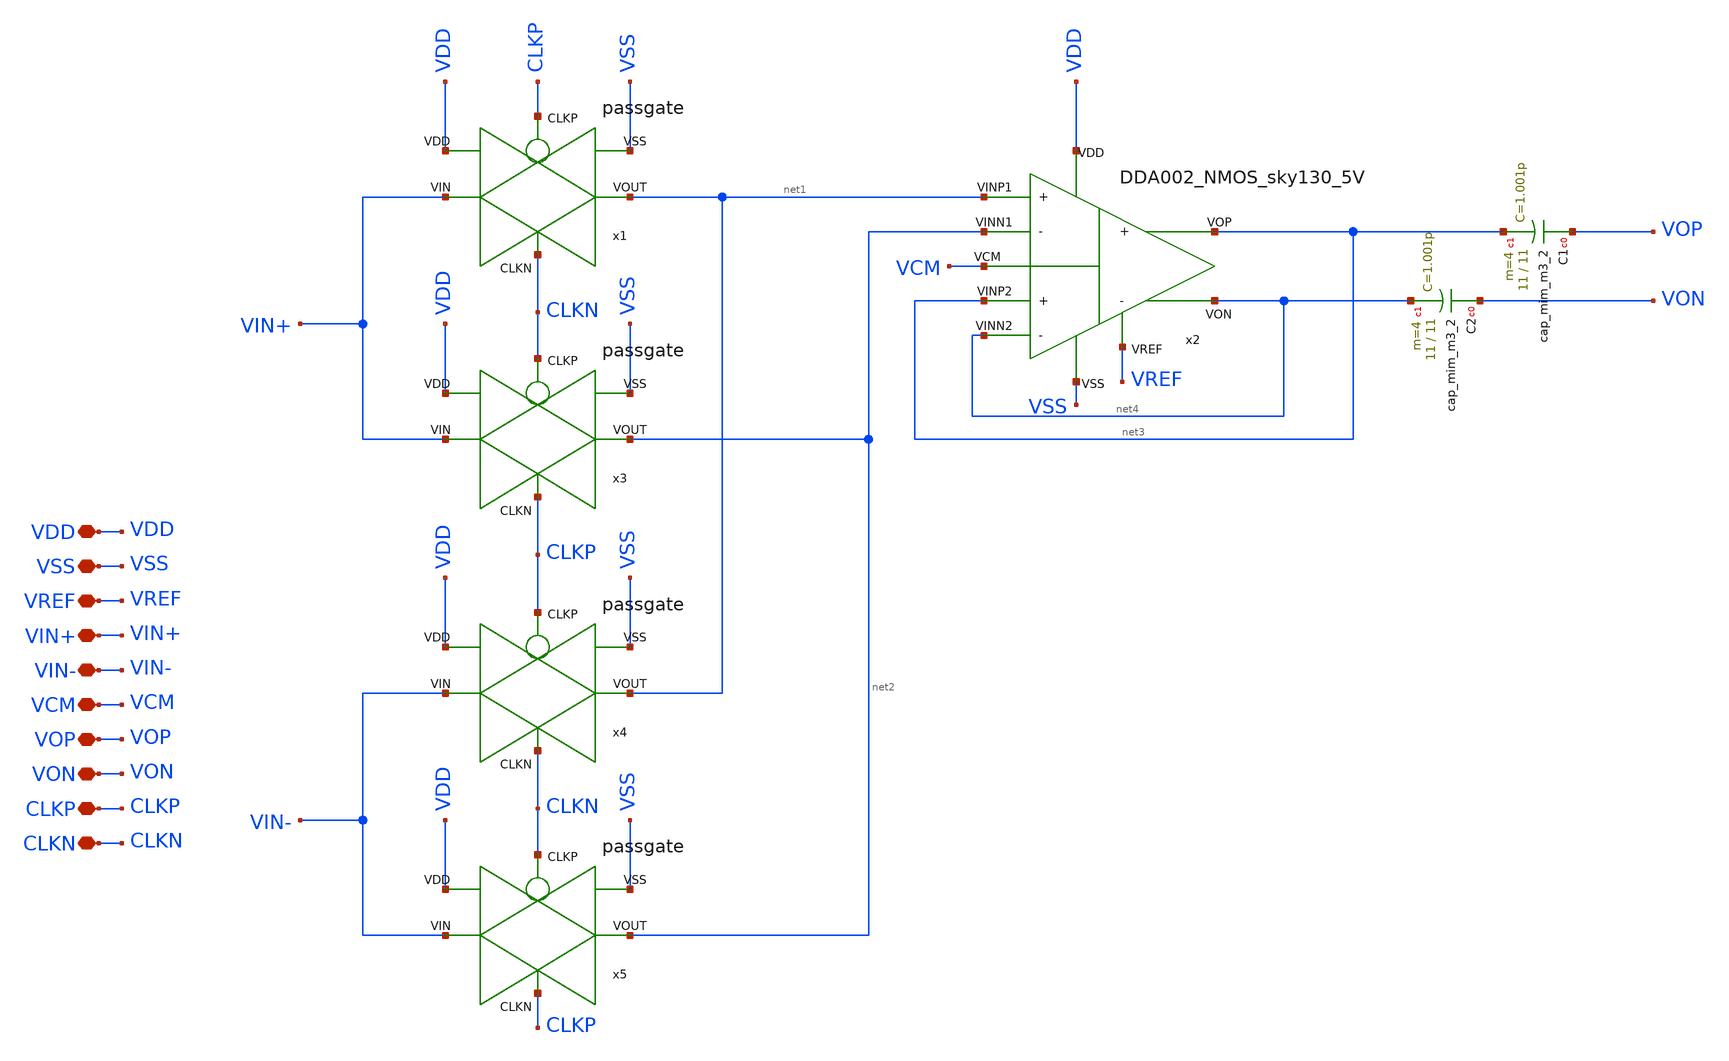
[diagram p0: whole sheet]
** sch_path: LIB/Sky130A/chopping/5v_sampling_chopping_buffer.sch
**.subckt 5v_sampling_chopping_buffer VDD VSS VREF VIN+ VIN- VCM VOP VON CLKP CLKN
*.iopin VDD
*.iopin VSS
*.iopin VREF
*.iopin VIN+
*.iopin VIN-
*.iopin VCM
*.iopin VOP
*.iopin VON
*.iopin CLKP
*.iopin CLKN
x2 VDD VSS VREF net2 net4 net1 net3 VCM net3 net4 DDA002_NMOS_sky130_5V
x1 VDD VSS VIN+ net1 CLKP CLKN passgate
x3 VDD VSS VIN+ net2 CLKN CLKP passgate
x4 VDD VSS VIN- net1 CLKP CLKN passgate
x5 VDD VSS VIN- net2 CLKN CLKP passgate
XC2 VON net4 sky130_fd_pr__cap_mim_m3_2 W=11 L=11 MF=4 m=4
XC1 VOP net3 sky130_fd_pr__cap_mim_m3_2 W=11 L=11 MF=4 m=4
**.ends

* expanding   symbol:  Sky130A/DDA/DDA002_NMOS_sky130_5V.sym # of pins=10
** sym_path: LIB/Sky130A/DDA/DDA002_NMOS_sky130_5V.sym
** sch_path: LIB/Sky130A/DDA/DDA002_NMOS_sky130_5V.sch
.subckt DDA002_NMOS_sky130_5V VDD VSS VREF VINN1 VINN2 VINP1 VINP2 VCM VOP VON
*.iopin VDD
*.iopin VSS
*.iopin VREF
*.iopin VINN1
*.iopin VINN2
*.iopin VINP1
*.iopin VINP2
*.iopin VCM
*.iopin VOP
*.iopin VON
XM2 VA2 VCMFB VDD VDD sky130_fd_pr__pfet_g5v0d10v5 L=2 W='1 * 2 ' nf=2 ad='int((2 + 1)/2) * 1 * 0.29'
+ as='int((2 + 2)/2) * 1 * 0.29' pd='2*int((2 + 1)/2) * (1 + 0.29)' ps='2*int((2 + 2)/2) * (1 + 0.29)'
+ nrd='0.29 / 1 / 2 ' nrs='0.29 / 1 / 2 ' sa=0 sb=0 sd=0 mult=2 m=2
XM3 VA1 VINP1 net1 VSS sky130_fd_pr__nfet_g5v0d10v5 L=1 W='3 * 2 ' nf=2 ad='int((nf+1)/2) * W / nf * 0.29'
+ as='int((nf+2)/2) * W / nf * 0.29' pd='2*int((nf+1)/2) * (W / nf + 0.29)' ps='2*int((nf+2)/2) * (W / nf + 0.29)'
+ nrd='0.29 / W ' nrs='0.29 / W ' sa=0 sb=0 sd=0 mult=4 m=4
XM13 net3 VB VSS VSS sky130_fd_pr__nfet_g5v0d10v5 L=3 W='1 * 2 ' nf=2 ad='int((nf+1)/2) * W / nf * 0.29'
+ as='int((nf+2)/2) * W / nf * 0.29' pd='2*int((nf+1)/2) * (W / nf + 0.29)' ps='2*int((nf+2)/2) * (W / nf + 0.29)'
+ nrd='0.29 / W ' nrs='0.29 / W ' sa=0 sb=0 sd=0 mult=2 m=2
XR1 net3 VB VSS sky130_fd_pr__res_high_po_0p35 L=26 mult=1 m=1
XM14 VB VREF VDD VDD sky130_fd_pr__pfet_g5v0d10v5 L=2.5 W='1 * 2 ' nf=2 ad='int((2 + 1)/2) * 1 * 0.29'
+ as='int((2 + 2)/2) * 1 * 0.29' pd='2*int((2 + 1)/2) * (1 + 0.29)' ps='2*int((2 + 2)/2) * (1 + 0.29)'
+ nrd='0.29 / 1 / 2 ' nrs='0.29 / 1 / 2 ' sa=0 sb=0 sd=0 mult=2 m=2
XM7 net1 VB VSS VSS sky130_fd_pr__nfet_g5v0d10v5 L=3 W='1 * 2 ' nf=2 ad='int((nf+1)/2) * W / nf * 0.29'
+ as='int((nf+2)/2) * W / nf * 0.29' pd='2*int((nf+1)/2) * (W / nf + 0.29)' ps='2*int((nf+2)/2) * (W / nf + 0.29)'
+ nrd='0.29 / W ' nrs='0.29 / W ' sa=0 sb=0 sd=0 mult=2 m=2
XM8 net2 VB VSS VSS sky130_fd_pr__nfet_g5v0d10v5 L=3 W='1 * 2 ' nf=2 ad='int((nf+1)/2) * W / nf * 0.29'
+ as='int((nf+2)/2) * W / nf * 0.29' pd='2*int((nf+1)/2) * (W / nf + 0.29)' ps='2*int((nf+2)/2) * (W / nf + 0.29)'
+ nrd='0.29 / W ' nrs='0.29 / W ' sa=0 sb=0 sd=0 mult=2 m=2
XM10 VON VB VSS VSS sky130_fd_pr__nfet_g5v0d10v5 L=3 W='1 * 2 ' nf=2 ad='int((nf+1)/2) * W / nf * 0.29'
+ as='int((nf+2)/2) * W / nf * 0.29' pd='2*int((nf+1)/2) * (W / nf + 0.29)' ps='2*int((nf+2)/2) * (W / nf + 0.29)'
+ nrd='0.29 / W ' nrs='0.29 / W ' sa=0 sb=0 sd=0 mult=4 m=4
XM12 VOP VB VSS VSS sky130_fd_pr__nfet_g5v0d10v5 L=3 W='1 * 2 ' nf=2 ad='int((nf+1)/2) * W / nf * 0.29'
+ as='int((nf+2)/2) * W / nf * 0.29' pd='2*int((nf+1)/2) * (W / nf + 0.29)' ps='2*int((nf+2)/2) * (W / nf + 0.29)'
+ nrd='0.29 / W ' nrs='0.29 / W ' sa=0 sb=0 sd=0 mult=4 m=4
XM1 VA1 VCMFB VDD VDD sky130_fd_pr__pfet_g5v0d10v5 L=2 W='1 * 2 ' nf=2 ad='int((2 + 1)/2) * 1 * 0.29'
+ as='int((2 + 2)/2) * 1 * 0.29' pd='2*int((2 + 1)/2) * (1 + 0.29)' ps='2*int((2 + 2)/2) * (1 + 0.29)'
+ nrd='0.29 / 1 / 2 ' nrs='0.29 / 1 / 2 ' sa=0 sb=0 sd=0 mult=2 m=2
XM6 VA2 VINN1 net1 VSS sky130_fd_pr__nfet_g5v0d10v5 L=1 W='3 * 2 ' nf=2 ad='int((nf+1)/2) * W / nf * 0.29'
+ as='int((nf+2)/2) * W / nf * 0.29' pd='2*int((nf+1)/2) * (W / nf + 0.29)' ps='2*int((nf+2)/2) * (W / nf + 0.29)'
+ nrd='0.29 / W ' nrs='0.29 / W ' sa=0 sb=0 sd=0 mult=4 m=4
XM5 VA2 VINN2 net2 VSS sky130_fd_pr__nfet_g5v0d10v5 L=1 W='3 * 2 ' nf=2 ad='int((nf+1)/2) * W / nf * 0.29'
+ as='int((nf+2)/2) * W / nf * 0.29' pd='2*int((nf+1)/2) * (W / nf + 0.29)' ps='2*int((nf+2)/2) * (W / nf + 0.29)'
+ nrd='0.29 / W ' nrs='0.29 / W ' sa=0 sb=0 sd=0 mult=4 m=4
XM4 VA1 VINP2 net2 VSS sky130_fd_pr__nfet_g5v0d10v5 L=1 W='3 * 2 ' nf=2 ad='int((nf+1)/2) * W / nf * 0.29'
+ as='int((nf+2)/2) * W / nf * 0.29' pd='2*int((nf+1)/2) * (W / nf + 0.29)' ps='2*int((nf+2)/2) * (W / nf + 0.29)'
+ nrd='0.29 / W ' nrs='0.29 / W ' sa=0 sb=0 sd=0 mult=4 m=4
XM9 VOP VA1 VDD VDD sky130_fd_pr__pfet_g5v0d10v5 L=0.7 W='5 * 4 ' nf=4 ad='int((4 + 1)/2) * 5 * 0.29'
+ as='int((4 + 2)/2) * 5 * 0.29' pd='2*int((4 + 1)/2) * (5 + 0.29)' ps='2*int((4 + 2)/2) * (5 + 0.29)'
+ nrd='0.29 / 5 / 4 ' nrs='0.29 / 5 / 4 ' sa=0 sb=0 sd=0 mult=4 m=4
XM11 VON VA2 VDD VDD sky130_fd_pr__pfet_g5v0d10v5 L=0.7 W='5 * 4 ' nf=4 ad='int((4 + 1)/2) * 5 * 0.29'
+ as='int((4 + 2)/2) * 5 * 0.29' pd='2*int((4 + 1)/2) * (5 + 0.29)' ps='2*int((4 + 2)/2) * (5 + 0.29)'
+ nrd='0.29 / 5 / 4 ' nrs='0.29 / 5 / 4 ' sa=0 sb=0 sd=0 mult=4 m=4
XC2 net4 VON sky130_fd_pr__cap_mim_m3_2 W=5.8 L=5.8 MF=4 m=4
XM15 net4 VB VA2 VDD sky130_fd_pr__pfet_g5v0d10v5 L=4 W='0.65 * 1 ' nf=1 ad='int((1 + 1)/2) * 0.65 * 0.29'
+ as='int((1 + 2)/2) * 0.65 * 0.29' pd='2*int((1 + 1)/2) * (0.65 + 0.29)' ps='2*int((1 + 2)/2) * (0.65 + 0.29)'
+ nrd='0.29 / 0.65 / 1 ' nrs='0.29 / 0.65 / 1 ' sa=0 sb=0 sd=0 mult=2 m=2
XM17 net6 VB VSS VSS sky130_fd_pr__nfet_g5v0d10v5 L=3 W='1 * 2 ' nf=2 ad='int((nf+1)/2) * W / nf * 0.29'
+ as='int((nf+2)/2) * W / nf * 0.29' pd='2*int((nf+1)/2) * (W / nf + 0.29)' ps='2*int((nf+2)/2) * (W / nf + 0.29)'
+ nrd='0.29 / W ' nrs='0.29 / W ' sa=0 sb=0 sd=0 mult=2 m=2
XM18 net7 VCM net6 VSS sky130_fd_pr__nfet_g5v0d10v5 L=0.7 W='3 * 2 ' nf=2 ad='int((nf+1)/2) * W / nf * 0.29'
+ as='int((nf+2)/2) * W / nf * 0.29' pd='2*int((nf+1)/2) * (W / nf + 0.29)' ps='2*int((nf+2)/2) * (W / nf + 0.29)'
+ nrd='0.29 / W ' nrs='0.29 / W ' sa=0 sb=0 sd=0 mult=4 m=4
XM19 VCMFB net8 net6 VSS sky130_fd_pr__nfet_g5v0d10v5 L=0.7 W='3 * 2 ' nf=2 ad='int((nf+1)/2) * W / nf * 0.29'
+ as='int((nf+2)/2) * W / nf * 0.29' pd='2*int((nf+1)/2) * (W / nf + 0.29)' ps='2*int((nf+2)/2) * (W / nf + 0.29)'
+ nrd='0.29 / W ' nrs='0.29 / W ' sa=0 sb=0 sd=0 mult=4 m=4
XM21 net7 net7 VDD VDD sky130_fd_pr__pfet_g5v0d10v5 L=3 W='1 * 2 ' nf=2 ad='int((2 + 1)/2) * 1 * 0.29'
+ as='int((2 + 2)/2) * 1 * 0.29' pd='2*int((2 + 1)/2) * (1 + 0.29)' ps='2*int((2 + 2)/2) * (1 + 0.29)'
+ nrd='0.29 / 1 / 2 ' nrs='0.29 / 1 / 2 ' sa=0 sb=0 sd=0 mult=2 m=2
XM20 VCMFB net7 VDD VDD sky130_fd_pr__pfet_g5v0d10v5 L=3 W='1 * 2 ' nf=2 ad='int((2 + 1)/2) * 1 * 0.29'
+ as='int((2 + 2)/2) * 1 * 0.29' pd='2*int((2 + 1)/2) * (1 + 0.29)' ps='2*int((2 + 2)/2) * (1 + 0.29)'
+ nrd='0.29 / 1 / 2 ' nrs='0.29 / 1 / 2 ' sa=0 sb=0 sd=0 mult=2 m=2
XC6 net10 VA1 sky130_fd_pr__cap_mim_m3_2 W=10 L=10 MF=8 m=8
XR7 net10 VCMFB VSS sky130_fd_pr__res_xhigh_po_0p35 L=10 mult=1 m=1
XC7 net9 VA2 sky130_fd_pr__cap_mim_m3_2 W=10 L=10 MF=8 m=8
XR6 net9 VCMFB VSS sky130_fd_pr__res_xhigh_po_0p35 L=10 mult=1 m=1
XR2 VON net8 VSS sky130_fd_pr__res_xhigh_po_0p35 L=50 mult=1 m=1
XR3 net8 VOP VSS sky130_fd_pr__res_xhigh_po_0p35 L=50 mult=1 m=1
XM16 net5 VB VA1 VDD sky130_fd_pr__pfet_g5v0d10v5 L=4 W='0.65 * 1 ' nf=1 ad='int((1 + 1)/2) * 0.65 * 0.29'
+ as='int((1 + 2)/2) * 0.65 * 0.29' pd='2*int((1 + 1)/2) * (0.65 + 0.29)' ps='2*int((1 + 2)/2) * (0.65 + 0.29)'
+ nrd='0.29 / 0.65 / 1 ' nrs='0.29 / 0.65 / 1 ' sa=0 sb=0 sd=0 mult=2 m=2
XC1 VOP net5 sky130_fd_pr__cap_mim_m3_2 W=5.8 L=5.8 MF=4 m=4
.ends


* expanding   symbol:  Sky130A/switches/passgate.sym # of pins=6
** sym_path: LIB/Sky130A/switches/passgate.sym
** sch_path: LIB/Sky130A/switches/passgate.sch
.subckt passgate VDD VSS VIN VOUT CLKP CLKN
*.iopin VDD
*.iopin VSS
*.iopin VIN
*.iopin VOUT
*.iopin CLKP
*.iopin CLKN
XM1 VIN CLKP VOUT VDD sky130_fd_pr__pfet_g5v0d10v5 L=0.5 W='1 * 3 ' nf=3 ad='int((3 + 1)/2) * 1 * 0.29'
+ as='int((3 + 2)/2) * 1 * 0.29' pd='2*int((3 + 1)/2) * (1 + 0.29)' ps='2*int((3 + 2)/2) * (1 + 0.29)'
+ nrd='0.29 / 1 / 3 ' nrs='0.29 / 1 / 3 ' sa=0 sb=0 sd=0 mult=1 m=1
XM37 VIN CLKN VOUT VSS sky130_fd_pr__nfet_g5v0d10v5 L=0.5 W='1 * 1 ' nf=1 ad='int((nf+1)/2) * W / nf * 0.29'
+ as='int((nf+2)/2) * W / nf * 0.29' pd='2*int((nf+1)/2) * (W / nf + 0.29)' ps='2*int((nf+2)/2) * (W / nf + 0.29)'
+ nrd='0.29 / W ' nrs='0.29 / W ' sa=0 sb=0 sd=0 mult=1 m=1
.ends

.end
